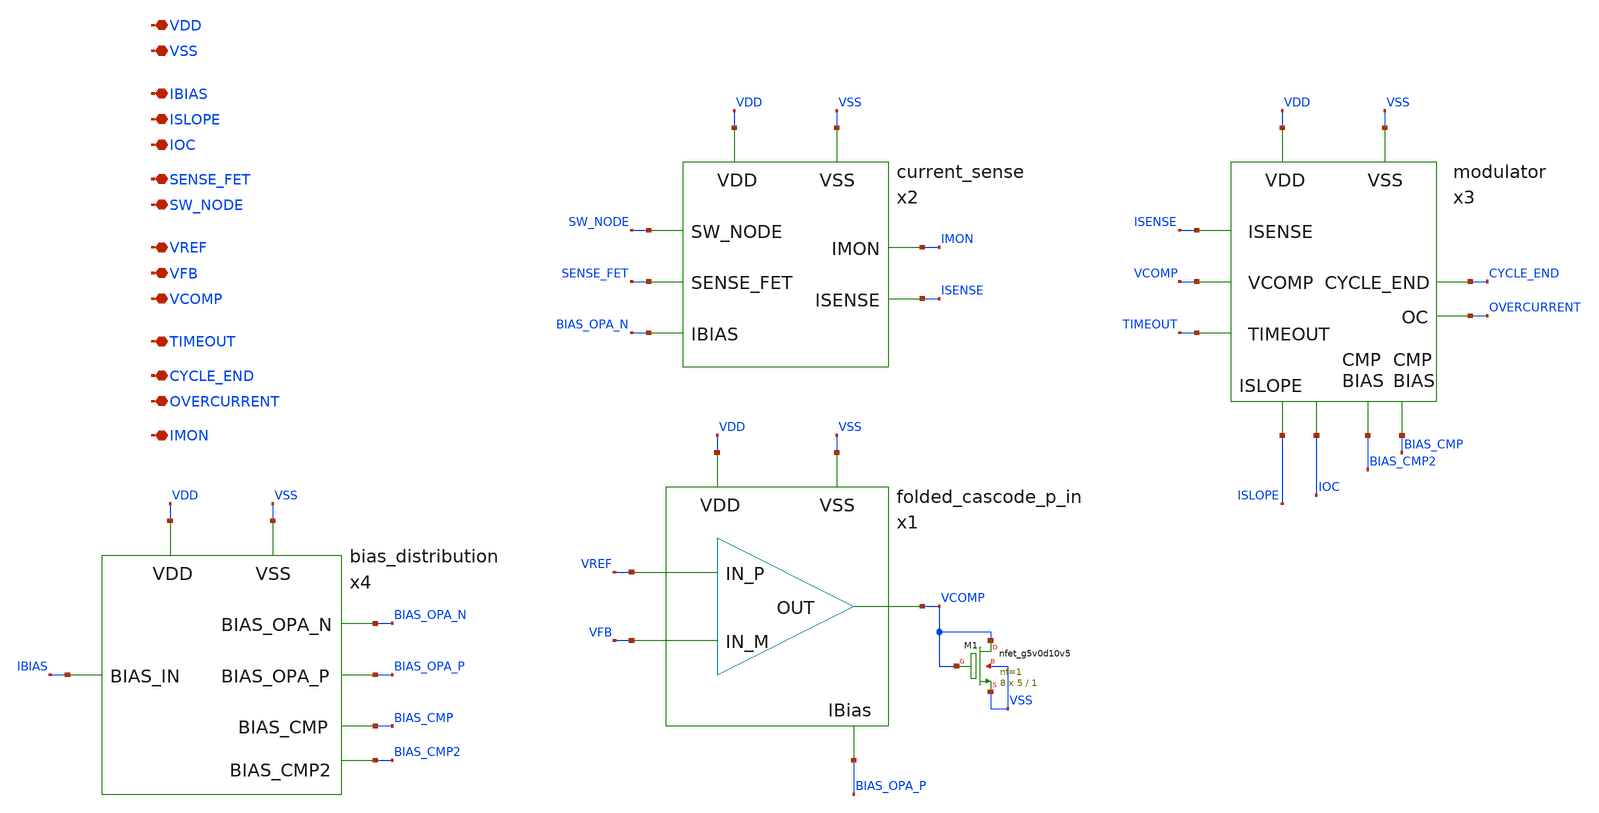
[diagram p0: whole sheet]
** sch_path: design/system/analog_subsystem.sch
**.subckt analog_subsystem VDD VSS IBIAS SENSE_FET SW_NODE ISLOPE VREF VFB VCOMP TIMEOUT CYCLE_END
*+ IMON IOC OVERCURRENT
*.iopin VDD
*.iopin VSS
*.iopin IBIAS
*.iopin SENSE_FET
*.iopin SW_NODE
*.iopin ISLOPE
*.iopin VREF
*.iopin VFB
*.iopin VCOMP
*.iopin TIMEOUT
*.iopin CYCLE_END
*.iopin IMON
*.iopin IOC
*.iopin OVERCURRENT
x1 VREF VFB VCOMP VDD VSS BIAS_OPA_P folded_cascode_p_in
x2 VDD VSS SW_NODE SENSE_FET BIAS_OPA_N IMON ISENSE current_sense
x3 VDD VSS BIAS_CMP ISLOPE ISENSE VCOMP TIMEOUT CYCLE_END BIAS_CMP2 IOC OVERCURRENT modulator
x4 VDD VSS IBIAS BIAS_OPA_N BIAS_OPA_P BIAS_CMP BIAS_CMP2 bias_distribution
XM1 VCOMP VCOMP VSS VSS sky130_fd_pr__nfet_g5v0d10v5 L=1 W=5 nf=1 ad='int((nf+1)/2) * W/nf * 0.29' as='int((nf+2)/2) * W/nf * 0.29'
+ pd='2*int((nf+1)/2) * (W/nf + 0.29)' ps='2*int((nf+2)/2) * (W/nf + 0.29)' nrd='0.29 / W' nrs='0.29 / W'
+ sa=0 sb=0 sd=0 mult=8 m=8
**.ends
.end
